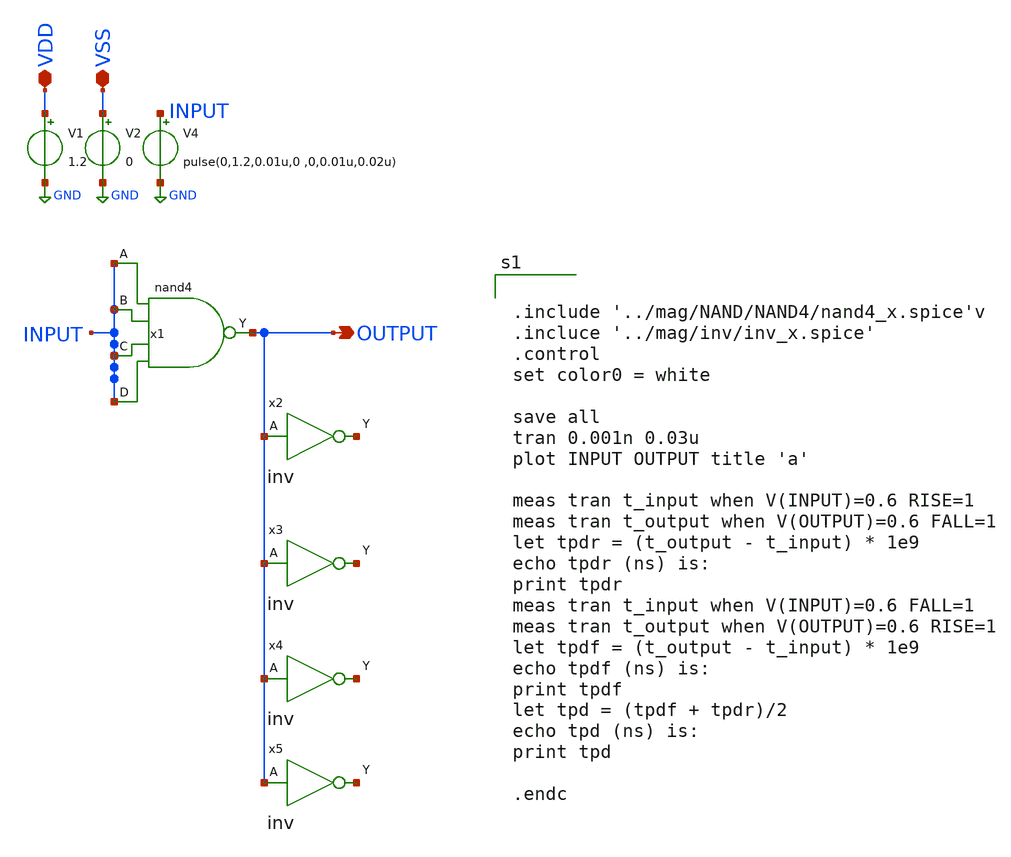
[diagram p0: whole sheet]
** sch_path: design/xschem/From Layout/NAND/nand_TB.sch
**.subckt nand_TB OUTPUT VDD VSS
*.opin OUTPUT
*.iopin VDD
*.iopin VSS
V1 VDD GND 1.2
V2 VSS GND 0
V4 INPUT GND pulse(0,1.2,0.01u,0 ,0,0.01u,0.02u)
x1 INPUT INPUT INPUT INPUT VSS VDD OUTPUT nand4
x2 OUTPUT VSS VDD net1 inv
x3 OUTPUT VSS VDD net2 inv
x4 OUTPUT VSS VDD net3 inv
x5 OUTPUT VSS VDD net4 inv
**** begin user architecture code

** opencircuitdesign pdks install
.lib $::SKYWATER_MODELS/sky130.lib.spice tt_mm




.include '../mag/NAND/NAND4/nand4_x.spice'v
.incluce '../mag/inv/inv_x.spice'
.control
set color0 = white

save all
tran 0.001n 0.03u
plot INPUT OUTPUT title 'a'

meas tran t_input when V(INPUT)=0.6 RISE=1
meas tran t_output when V(OUTPUT)=0.6 FALL=1
let tpdr = (t_output - t_input) * 1e9
echo tpdr (ns) is:
print tpdr
meas tran t_input when V(INPUT)=0.6 FALL=1
meas tran t_output when V(OUTPUT)=0.6 RISE=1
let tpdf = (t_output - t_input) * 1e9
echo tpdf (ns) is:
print tpdf
let tpd = (tpdf + tpdr)/2
echo tpd (ns) is:
print tpd

.endc


**** end user architecture code
**.ends
.GLOBAL GND
.end
